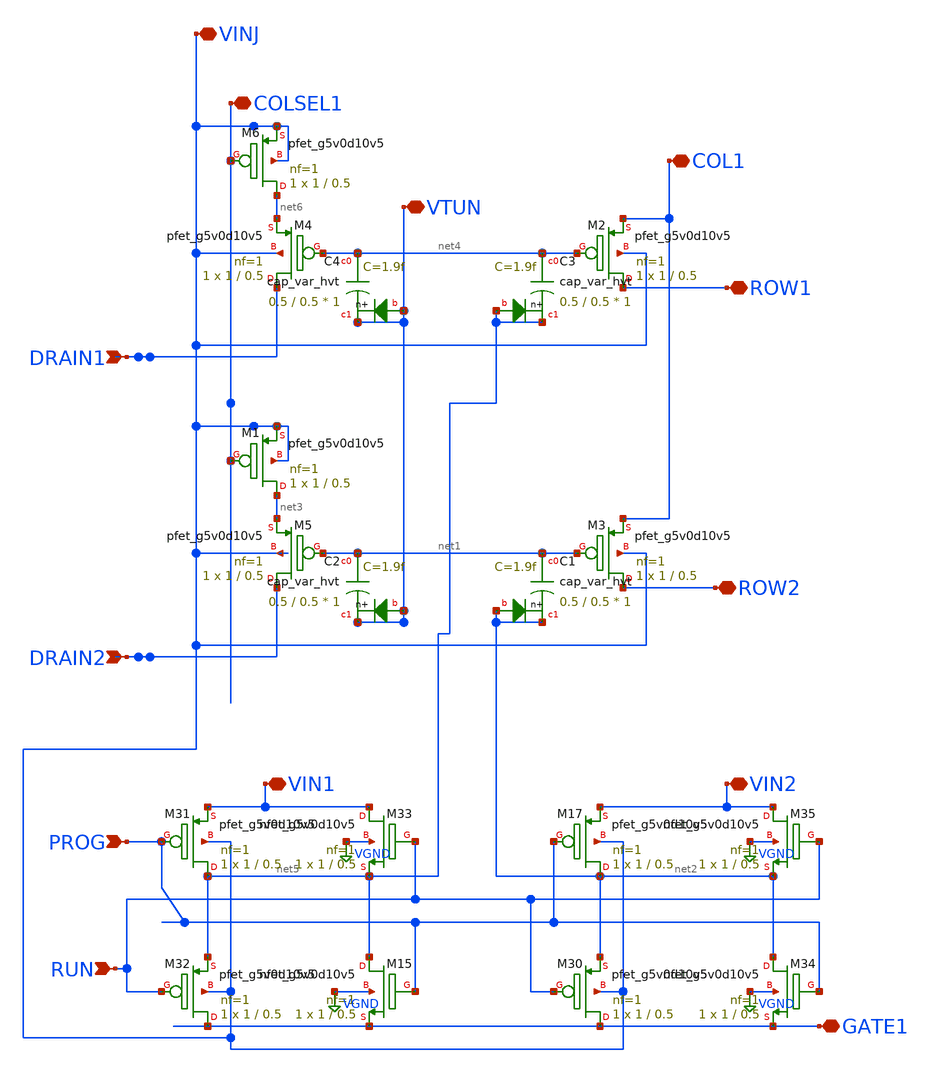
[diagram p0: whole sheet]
** sch_path: libs.ref/sky130_hilas_sc/xschem/sky130_hilas_FGtrans2x1cell.sch
**.subckt sky130_hilas_FGtrans2x1cell DRAIN1 DRAIN2 RUN PROG VTUN COLSEL1 VINJ GATE1 VIN1 VIN2 COL1
*+ ROW2 ROW1
*.ipin DRAIN1
*.ipin DRAIN2
*.ipin RUN
*.ipin PROG
*.iopin VTUN
*.iopin COLSEL1
*.iopin VINJ
*.iopin GATE1
*.iopin VIN1
*.iopin VIN2
*.iopin COL1
*.iopin ROW2
*.iopin ROW1
XM3 ROW2 net1 COL1 VINJ sky130_fd_pr__pfet_g5v0d10v5 L=0.5 W=1 nf=1 ad='int((nf+1)/2) * W/nf * 0.29'
+ as='int((nf+2)/2) * W/nf * 0.29' pd='2*int((nf+1)/2) * (W/nf + 0.29)' ps='2*int((nf+2)/2) * (W/nf + 0.29)'
+ nrd='0.29 / W' nrs='0.29 / W' sa=0 sb=0 sd=0 mult=1 m=1
XC1 net1 net2 net2 sky130_fd_pr__cap_var_hvt W=0.5 L=0.5 VM=1 m=1
XM5 DRAIN2 net1 net3 VINJ sky130_fd_pr__pfet_g5v0d10v5 L=0.5 W=1 nf=1 ad='int((nf+1)/2) * W/nf * 0.29'
+ as='int((nf+2)/2) * W/nf * 0.29' pd='2*int((nf+1)/2) * (W/nf + 0.29)' ps='2*int((nf+2)/2) * (W/nf + 0.29)'
+ nrd='0.29 / W' nrs='0.29 / W' sa=0 sb=0 sd=0 mult=1 m=1
XC2 net1 VTUN VTUN sky130_fd_pr__cap_var_hvt W=0.5 L=0.5 VM=1 m=1
XM1 net3 COLSEL1 VINJ VINJ sky130_fd_pr__pfet_g5v0d10v5 L=0.5 W=1 nf=1 ad='int((nf+1)/2) * W/nf * 0.29'
+ as='int((nf+2)/2) * W/nf * 0.29' pd='2*int((nf+1)/2) * (W/nf + 0.29)' ps='2*int((nf+2)/2) * (W/nf + 0.29)'
+ nrd='0.29 / W' nrs='0.29 / W' sa=0 sb=0 sd=0 mult=1 m=1
XM2 ROW1 net4 COL1 VINJ sky130_fd_pr__pfet_g5v0d10v5 L=0.5 W=1 nf=1 ad='int((nf+1)/2) * W/nf * 0.29'
+ as='int((nf+2)/2) * W/nf * 0.29' pd='2*int((nf+1)/2) * (W/nf + 0.29)' ps='2*int((nf+2)/2) * (W/nf + 0.29)'
+ nrd='0.29 / W' nrs='0.29 / W' sa=0 sb=0 sd=0 mult=1 m=1
XC3 net4 net5 net5 sky130_fd_pr__cap_var_hvt W=0.5 L=0.5 VM=1 m=1
XM4 DRAIN1 net4 net6 VINJ sky130_fd_pr__pfet_g5v0d10v5 L=0.5 W=1 nf=1 ad='int((nf+1)/2) * W/nf * 0.29'
+ as='int((nf+2)/2) * W/nf * 0.29' pd='2*int((nf+1)/2) * (W/nf + 0.29)' ps='2*int((nf+2)/2) * (W/nf + 0.29)'
+ nrd='0.29 / W' nrs='0.29 / W' sa=0 sb=0 sd=0 mult=1 m=1
XC4 net4 VTUN VTUN sky130_fd_pr__cap_var_hvt W=0.5 L=0.5 VM=1 m=1
XM6 net6 COLSEL1 VINJ VINJ sky130_fd_pr__pfet_g5v0d10v5 L=0.5 W=1 nf=1 ad='int((nf+1)/2) * W/nf * 0.29'
+ as='int((nf+2)/2) * W/nf * 0.29' pd='2*int((nf+1)/2) * (W/nf + 0.29)' ps='2*int((nf+2)/2) * (W/nf + 0.29)'
+ nrd='0.29 / W' nrs='0.29 / W' sa=0 sb=0 sd=0 mult=1 m=1
XM15 net5 PROG GATE1 VGND sky130_fd_pr__nfet_g5v0d10v5 L=0.5 W=1 nf=1 ad='int((nf+1)/2) * W/nf * 0.29'
+ as='int((nf+2)/2) * W/nf * 0.29' pd='2*int((nf+1)/2) * (W/nf + 0.29)' ps='2*int((nf+2)/2) * (W/nf + 0.29)'
+ nrd='0.29 / W' nrs='0.29 / W' sa=0 sb=0 sd=0 mult=1 m=1
XM17 net2 PROG VIN2 VINJ sky130_fd_pr__pfet_g5v0d10v5 L=0.5 W=1 nf=1 ad='int((nf+1)/2) * W/nf * 0.29'
+ as='int((nf+2)/2) * W/nf * 0.29' pd='2*int((nf+1)/2) * (W/nf + 0.29)' ps='2*int((nf+2)/2) * (W/nf + 0.29)'
+ nrd='0.29 / W' nrs='0.29 / W' sa=0 sb=0 sd=0 mult=1 m=1
XM30 GATE1 RUN net2 VINJ sky130_fd_pr__pfet_g5v0d10v5 L=0.5 W=1 nf=1 ad='int((nf+1)/2) * W/nf * 0.29'
+ as='int((nf+2)/2) * W/nf * 0.29' pd='2*int((nf+1)/2) * (W/nf + 0.29)' ps='2*int((nf+2)/2) * (W/nf + 0.29)'
+ nrd='0.29 / W' nrs='0.29 / W' sa=0 sb=0 sd=0 mult=1 m=1
XM31 net5 PROG VIN1 VINJ sky130_fd_pr__pfet_g5v0d10v5 L=0.5 W=1 nf=1 ad='int((nf+1)/2) * W/nf * 0.29'
+ as='int((nf+2)/2) * W/nf * 0.29' pd='2*int((nf+1)/2) * (W/nf + 0.29)' ps='2*int((nf+2)/2) * (W/nf + 0.29)'
+ nrd='0.29 / W' nrs='0.29 / W' sa=0 sb=0 sd=0 mult=1 m=1
XM32 GATE1 RUN net5 VINJ sky130_fd_pr__pfet_g5v0d10v5 L=0.5 W=1 nf=1 ad='int((nf+1)/2) * W/nf * 0.29'
+ as='int((nf+2)/2) * W/nf * 0.29' pd='2*int((nf+1)/2) * (W/nf + 0.29)' ps='2*int((nf+2)/2) * (W/nf + 0.29)'
+ nrd='0.29 / W' nrs='0.29 / W' sa=0 sb=0 sd=0 mult=1 m=1
XM33 VIN1 RUN net5 VGND sky130_fd_pr__nfet_g5v0d10v5 L=0.5 W=1 nf=1 ad='int((nf+1)/2) * W/nf * 0.29'
+ as='int((nf+2)/2) * W/nf * 0.29' pd='2*int((nf+1)/2) * (W/nf + 0.29)' ps='2*int((nf+2)/2) * (W/nf + 0.29)'
+ nrd='0.29 / W' nrs='0.29 / W' sa=0 sb=0 sd=0 mult=1 m=1
XM34 net2 PROG GATE1 VGND sky130_fd_pr__nfet_g5v0d10v5 L=0.5 W=1 nf=1 ad='int((nf+1)/2) * W/nf * 0.29'
+ as='int((nf+2)/2) * W/nf * 0.29' pd='2*int((nf+1)/2) * (W/nf + 0.29)' ps='2*int((nf+2)/2) * (W/nf + 0.29)'
+ nrd='0.29 / W' nrs='0.29 / W' sa=0 sb=0 sd=0 mult=1 m=1
XM35 VIN2 RUN net2 VGND sky130_fd_pr__nfet_g5v0d10v5 L=0.5 W=1 nf=1 ad='int((nf+1)/2) * W/nf * 0.29'
+ as='int((nf+2)/2) * W/nf * 0.29' pd='2*int((nf+1)/2) * (W/nf + 0.29)' ps='2*int((nf+2)/2) * (W/nf + 0.29)'
+ nrd='0.29 / W' nrs='0.29 / W' sa=0 sb=0 sd=0 mult=1 m=1
**.ends
.GLOBAL VGND
.end
